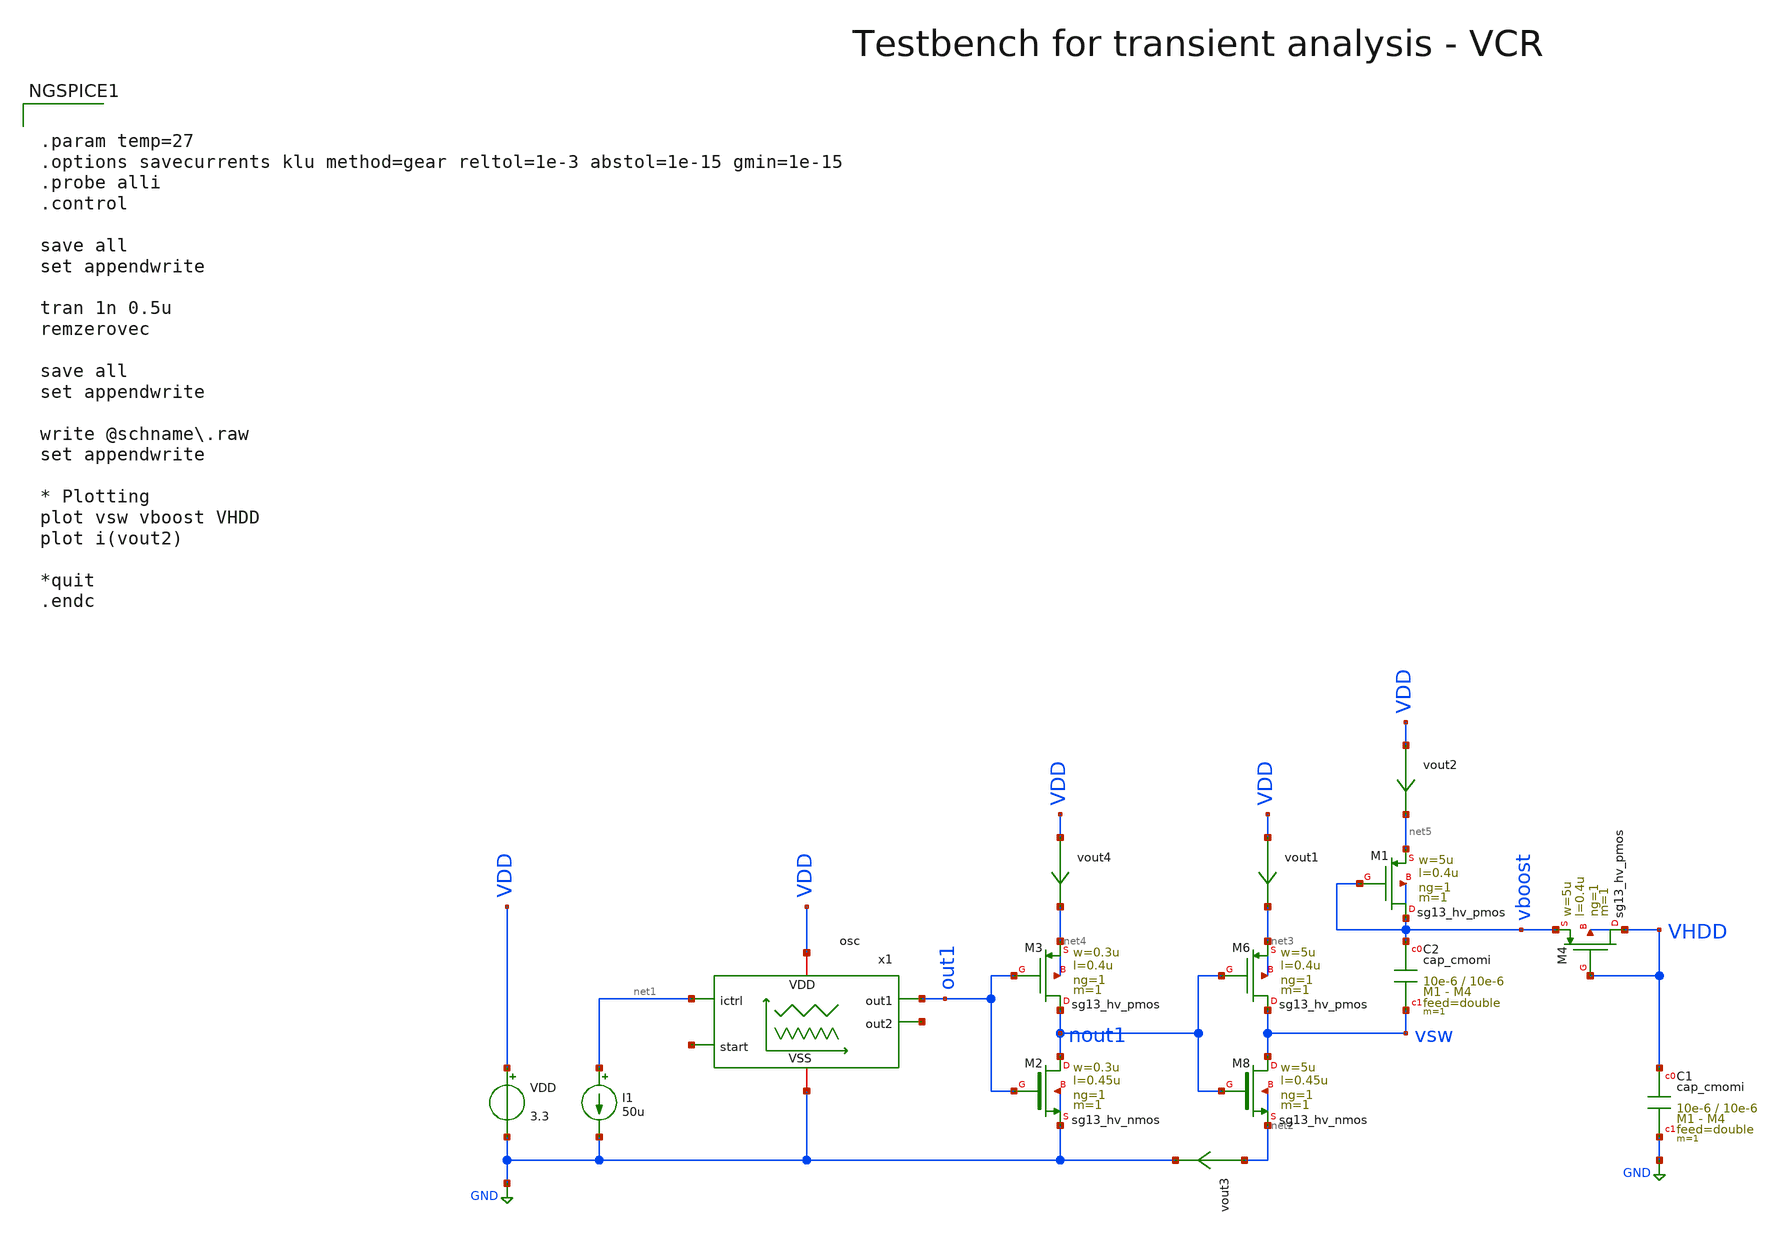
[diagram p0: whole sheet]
** sch_path: macros/heichips26_vcr/macros/switched_capacitor/testbenches/xschem/tb_chargepump_tran.sch
**.subckt tb_chargepump_tran
VDD VDD GND 3.3
I1 net1 GND 50u
x1 VDD out1 net1 GND net6 net7 osc
XM8 vsw nout1 net2 net2 sg13_hv_nmos w=5u l=0.45u ng=1 m=1 mm_ok=1
XM6 vsw nout1 net3 net3 sg13_hv_pmos w=5u l=0.4u ng=1 m=1 mm_ok=1
XC2 vboost vsw cap_cmomi w=10e-6 l=10e-6 mmin=1 mmax=4 feed=double subblock=0 m=1 mm_ok=1
vout1 VDD net3 0
.save i(vout1)
vout2 VDD net5 0
.save i(vout2)
vout3 net2 GND 0
.save i(vout3)
XM2 nout1 out1 GND GND sg13_hv_nmos w=0.3u l=0.45u ng=1 m=1 mm_ok=1
XM3 nout1 out1 net4 net4 sg13_hv_pmos w=0.3u l=0.4u ng=1 m=1 mm_ok=1
vout4 VDD net4 0
.save i(vout4)
XM1 vboost vboost net5 vboost sg13_hv_pmos w=5u l=0.4u ng=1 m=1 mm_ok=1
XC1 VHDD GND cap_cmomi w=10e-6 l=10e-6 mmin=1 mmax=4 feed=double subblock=0 m=1 mm_ok=1
XM4 VHDD VHDD vboost VHDD sg13_hv_pmos w=5u l=0.4u ng=1 m=1 mm_ok=1
**** begin user architecture code

.lib cornerMOSlv.lib mos_tt
.lib cornerMOShv.lib mos_tt
.lib cornerRES.lib res_typ
.lib cornerDIO.lib dio_tt
.lib cornerCAP.lib cap_typ

.include $::PDK_ROOT/$::PDK/libs.ref/sg13cmos5l_stdcell/spice/sg13cmos5l_stdcell.spice



.param temp=27
.options savecurrents klu method=gear reltol=1e-3 abstol=1e-15 gmin=1e-15
.probe alli
.control

save all
set appendwrite

tran 1n 0.5u
remzerovec

save all
set appendwrite

write @schname\.raw
set appendwrite

* Plotting
plot vsw vboost VHDD
plot i(vout2)

*quit
.endc


**** end user architecture code
**.ends

* expanding   symbol:  osc.sym # of pins=6
** sym_path: macros/heichips26_vcr/macros/switched_capacitor/schematic/xschem/osc.sym
** sch_path: macros/heichips26_vcr/macros/switched_capacitor/schematic/xschem/osc.sch
.subckt osc VDD out1 ictrl VSS start out2
*.iopin VSS
*.iopin VDD
*.iopin out2
*.iopin out1
*.iopin start
*.iopin ictrl
XM3 out1 ictrl VDD VDD sg13_hv_pmos w=10.0u l=2.0u ng=1 m=1 mm_ok=1
XM2 net1 ictrl VDD VDD sg13_hv_pmos w=1u l=2.0u ng=1 m=1 mm_ok=1
XM4 start ictrl VDD VDD sg13_hv_pmos w=1.0u l=2.0u ng=1 m=1 mm_ok=1
XM5 out2 ictrl VDD VDD sg13_hv_pmos w=10.0u l=2.0u ng=1 m=1 mm_ok=1
XM6 ictrl ictrl VDD VDD sg13_hv_pmos w=10.0u l=2.0u ng=1 m=1 mm_ok=1
XC1 net1 out1 cap_cmomi w=10e-6 l=10e-6 mmin=1 mmax=4 feed=double subblock=0 m=1 mm_ok=1
XC2 out2 start cap_cmomi w=10e-6 l=10e-6 mmin=1 mmax=4 feed=double subblock=0 m=1 mm_ok=1
XM8 out1 start VSS VSS sg13_hv_nmos w=3u l=0.45u ng=1 m=1 mm_ok=1
XM1 start start VSS VSS sg13_hv_nmos w=1u l=2u ng=1 m=1 mm_ok=1
XM12 out2 net1 VSS VSS sg13_hv_nmos w=3u l=0.45u ng=1 m=1 mm_ok=1
XM11 net1 net1 VSS VSS sg13_hv_nmos w=1u l=2u ng=1 m=1 mm_ok=1
**** begin user architecture code


.ic v(out1)=0 v(out2)=3.3


**** end user architecture code
.ends

.GLOBAL GND
.end
